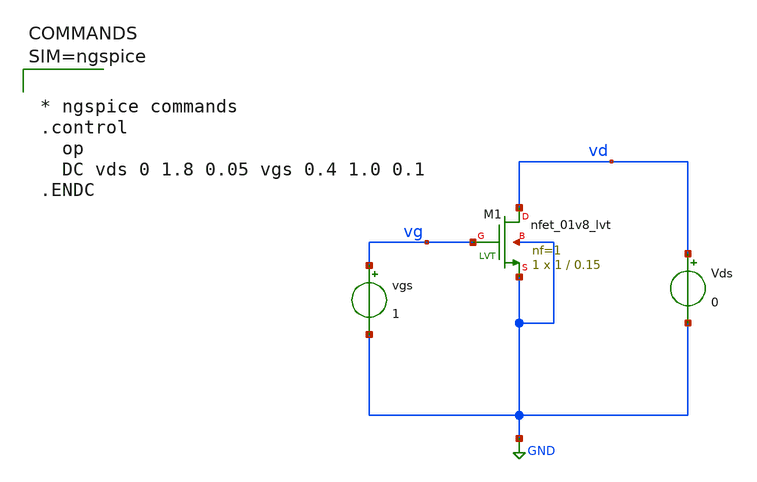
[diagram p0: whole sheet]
** sch_path: xschem/nmos.sch
**.subckt nmos
XM1 vd vg GND GND sky130_fd_pr__nfet_01v8_lvt L=0.15 W=1 nf=1 ad='int((1 + 1)/2) * 1 / 1 * 0.29' as='int((1 + 2)/2) * 1 / 1 * 0.29'
+ pd='2*int((1 + 1)/2) * (1 / 1 + 0.29)' ps='2*int((1 + 2)/2) * (1 / 1 + 0.29)' nrd='0.29 / 1 ' nrs='0.29 / 1 '
+ sa=0 sb=0 sd=0 mult=1 m=1
vgs vg GND 1
Vds vd GND 0
**** begin user architecture code

** opencircuitdesign pdks install
.lib $::SKYWATER_MODELS/sky130.lib.spice tt




* ngspice commands
.control
  op
  DC vds 0 1.8 0.05 vgs 0.4 1.0 0.1
.ENDC



**** end user architecture code
**.ends
.GLOBAL GND
.end
